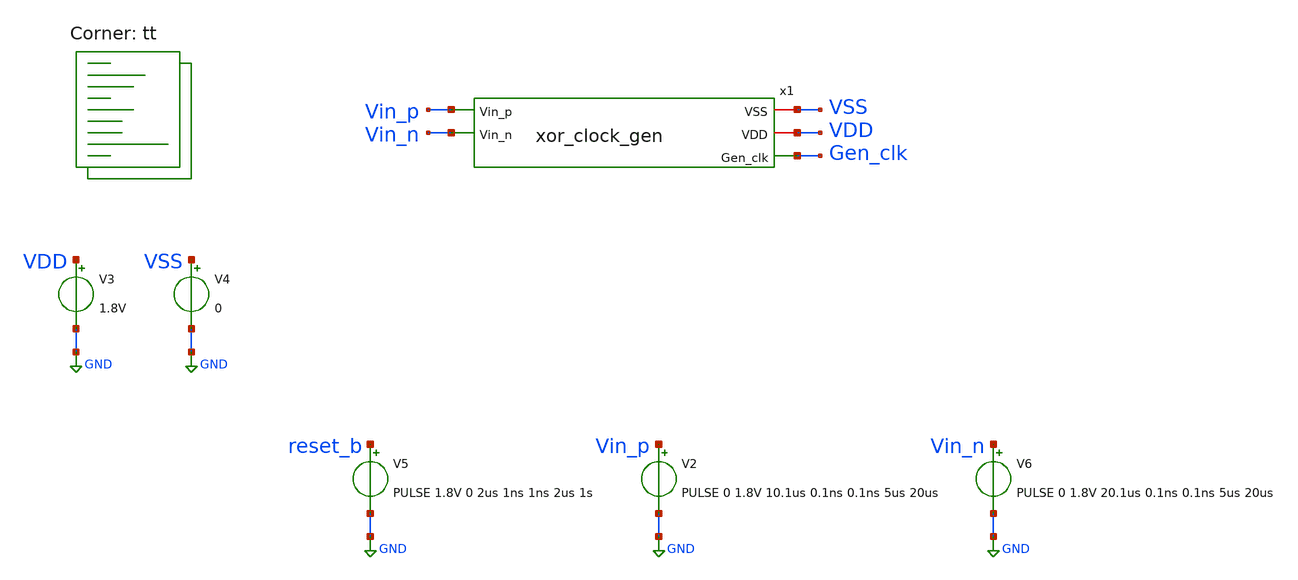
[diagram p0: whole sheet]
** sch_path: xschem/tests/xor_clock_gen/xor_clock_gen_test.sch
**.subckt xor_clock_gen_test
V3 VDD GND 1.8V
V4 VSS GND 0
x1 VSS Vin_p VDD Vin_n Gen_clk xor_clock_gen
V5 reset_b GND PULSE 1.8V 0 2us 1ns 1ns 2us 1s
V2 Vin_p GND PULSE 0 1.8V 10.1us 0.1ns 0.1ns 5us 20us
V6 Vin_n GND PULSE 0 1.8V 20.1us 0.1ns 0.1ns 5us 20us
**** begin user architecture code
 *.lib $::SKYWATER_MODELS/sky130.lib.spice tt
.include $::SKYWATER_STDCELLS/sky130_fd_sc_hd.spice


.options acct list
.options method=gear
.temp 25
*vvcc VDD 0 dc 1.8
*vvss VSS 0 0
.control
save all
tran 0.01u 80u
*plot RST_PLS clk+2 Pulse+4
plot Vin_p-Vin_n reset_b-2 Gen_clk+2
write xor_clock_gen_test.raw
.endc


.lib $::SKYWATER_MODELS/sky130.lib.spice tt
**** end user architecture code
**.ends

* expanding   symbol:  src/xor_clock_gen/xor_clock_gen.sym # of pins=5
** sym_path: xschem/src/xor_clock_gen/xor_clock_gen.sym
** sch_path: xschem/src/xor_clock_gen/xor_clock_gen.sch
.subckt xor_clock_gen VSS Vin_p VDD Vin_n Gen_clk
*.ipin Vin_p
*.iopin VSS
*.opin Gen_clk
*.iopin VDD
*.ipin Vin_n
x2 Vin_p Vin_n VSS VSS VDD VDD net1 sky130_fd_sc_hd__xor2_1
x3 net1 VSS VSS VDD VDD net2 sky130_fd_sc_hd__clkdlybuf4s50_1
x17 net2 VSS VSS VDD VDD net3 sky130_fd_sc_hd__clkdlybuf4s50_1
x9 net14 VSS VSS VDD VDD net4 sky130_fd_sc_hd__clkbuf_1
x14 net4 VSS VSS VDD VDD net5 sky130_fd_sc_hd__clkbuf_2
x19 net5 VSS VSS VDD VDD net6 sky130_fd_sc_hd__clkbuf_4
x26 net6 VSS VSS VDD VDD net7 sky130_fd_sc_hd__clkbuf_8
x27 net7 VSS VSS VDD VDD Gen_clk sky130_fd_sc_hd__clkbuf_16
XC1 net7 VSS sky130_fd_pr__cap_mim_m3_1 W=3 L=3 MF=3 m=3
x1 net3 VSS VSS VDD VDD net9 sky130_fd_sc_hd__clkdlybuf4s50_1
x4 net9 VSS VSS VDD VDD net8 sky130_fd_sc_hd__clkdlybuf4s50_1
x5 net8 VSS VSS VDD VDD net10 sky130_fd_sc_hd__clkdlybuf4s50_1
x7 net11 VSS VSS VDD VDD net15 sky130_fd_sc_hd__clkdlybuf4s50_1
x8 net15 VSS VSS VDD VDD net16 sky130_fd_sc_hd__clkdlybuf4s50_1
x10 net16 VSS VSS VDD VDD net17 sky130_fd_sc_hd__clkdlybuf4s50_1
x11 net17 VSS VSS VDD VDD net19 sky130_fd_sc_hd__clkdlybuf4s50_1
x12 net20 VSS VSS VDD VDD net21 sky130_fd_sc_hd__clkdlybuf4s50_1
x13 net21 VSS VSS VDD VDD net12 sky130_fd_sc_hd__clkdlybuf4s50_1
x15 net12 VSS VSS VDD VDD net13 sky130_fd_sc_hd__clkdlybuf4s50_1
x16 net13 VSS VSS VDD VDD net22 sky130_fd_sc_hd__clkdlybuf4s50_1
x18 net22 VSS VSS VDD VDD net14 sky130_fd_sc_hd__clkdlybuf4s50_1
x6 net10 VSS VSS VDD VDD net11 sky130_fd_sc_hd__clkdlybuf4s50_1
x20 net19 VSS VSS VDD VDD net18 sky130_fd_sc_hd__clkdlybuf4s50_1
x21 net18 VSS VSS VDD VDD net20 sky130_fd_sc_hd__clkdlybuf4s50_1
.ends

.GLOBAL GND
.end
